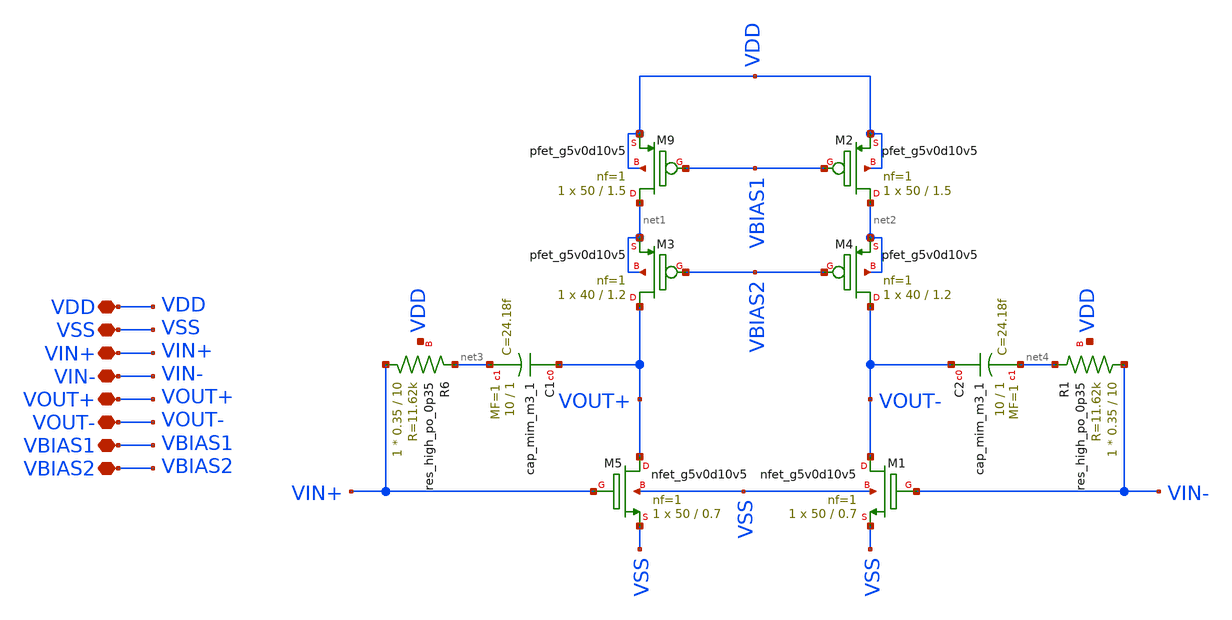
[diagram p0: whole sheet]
** sch_path: old stuff/folded_cascode_amplifier_upgraded/2_stage/second_stage.sch
**.subckt second_stage VDD VSS VIN+ VIN- VOUT+ VOUT- VBIAS1 VBIAS2
*.iopin VDD
*.iopin VSS
*.iopin VIN+
*.iopin VIN-
*.iopin VOUT+
*.iopin VOUT-
*.iopin VBIAS1
*.iopin VBIAS2
XM5 VOUT+ VIN+ VSS VSS sky130_fd_pr__nfet_g5v0d10v5 L=0.7 W=50 nf=1 ad='int((1 + 1)/2) * 50 / 1 * 0.29'
+ as='int((1 + 2)/2) * 50 / 1 * 0.29' pd='2*int((1 + 1)/2) * (50 / 1 + 0.29)' ps='2*int((1 + 2)/2) * (50 / 1 + 0.29)'
+ nrd='0.29 / 50 ' nrs='0.29 / 50 ' sa=0 sb=0 sd=0 mult=1 m=1
XM1 VOUT- VIN- VSS VSS sky130_fd_pr__nfet_g5v0d10v5 L=0.7 W=50 nf=1 ad='int((1 + 1)/2) * 50 / 1 * 0.29'
+ as='int((1 + 2)/2) * 50 / 1 * 0.29' pd='2*int((1 + 1)/2) * (50 / 1 + 0.29)' ps='2*int((1 + 2)/2) * (50 / 1 + 0.29)'
+ nrd='0.29 / 50 ' nrs='0.29 / 50 ' sa=0 sb=0 sd=0 mult=1 m=1
XM9 net1 VBIAS1 VDD VDD sky130_fd_pr__pfet_g5v0d10v5 L=1.5 W=50 nf=1 ad='int((1 + 1)/2) * 50 / 1 * 0.29'
+ as='int((1 + 2)/2) * 50 / 1 * 0.29' pd='2*int((1 + 1)/2) * (50 / 1 + 0.29)' ps='2*int((1 + 2)/2) * (50 / 1 + 0.29)'
+ nrd='0.29 / 50 ' nrs='0.29 / 50 ' sa=0 sb=0 sd=0 mult=1 m=1
XM2 net2 VBIAS1 VDD VDD sky130_fd_pr__pfet_g5v0d10v5 L=1.5 W=50 nf=1 ad='int((1 + 1)/2) * 50 / 1 * 0.29'
+ as='int((1 + 2)/2) * 50 / 1 * 0.29' pd='2*int((1 + 1)/2) * (50 / 1 + 0.29)' ps='2*int((1 + 2)/2) * (50 / 1 + 0.29)'
+ nrd='0.29 / 50 ' nrs='0.29 / 50 ' sa=0 sb=0 sd=0 mult=1 m=1
XM3 VOUT+ VBIAS2 net1 net1 sky130_fd_pr__pfet_g5v0d10v5 L=1.2 W=40 nf=1 ad='int((1 + 1)/2) * 40 / 1 * 0.29'
+ as='int((1 + 2)/2) * 40 / 1 * 0.29' pd='2*int((1 + 1)/2) * (40 / 1 + 0.29)' ps='2*int((1 + 2)/2) * (40 / 1 + 0.29)'
+ nrd='0.29 / 40 ' nrs='0.29 / 40 ' sa=0 sb=0 sd=0 mult=1 m=1
XM4 VOUT- VBIAS2 net2 net2 sky130_fd_pr__pfet_g5v0d10v5 L=1.2 W=40 nf=1 ad='int((1 + 1)/2) * 40 / 1 * 0.29'
+ as='int((1 + 2)/2) * 40 / 1 * 0.29' pd='2*int((1 + 1)/2) * (40 / 1 + 0.29)' ps='2*int((1 + 2)/2) * (40 / 1 + 0.29)'
+ nrd='0.29 / 40 ' nrs='0.29 / 40 ' sa=0 sb=0 sd=0 mult=1 m=1
XC1 VOUT+ net3 sky130_fd_pr__cap_mim_m3_1 W=10 L=1 MF=1 m=1
XR6 VIN+ net3 VDD sky130_fd_pr__res_high_po_0p35 L=10 mult=1 m=1
XC2 VOUT- net4 sky130_fd_pr__cap_mim_m3_1 W=10 L=1 MF=1 m=1
XR1 VIN- net4 VDD sky130_fd_pr__res_high_po_0p35 L=10 mult=1 m=1
**.ends
.end
